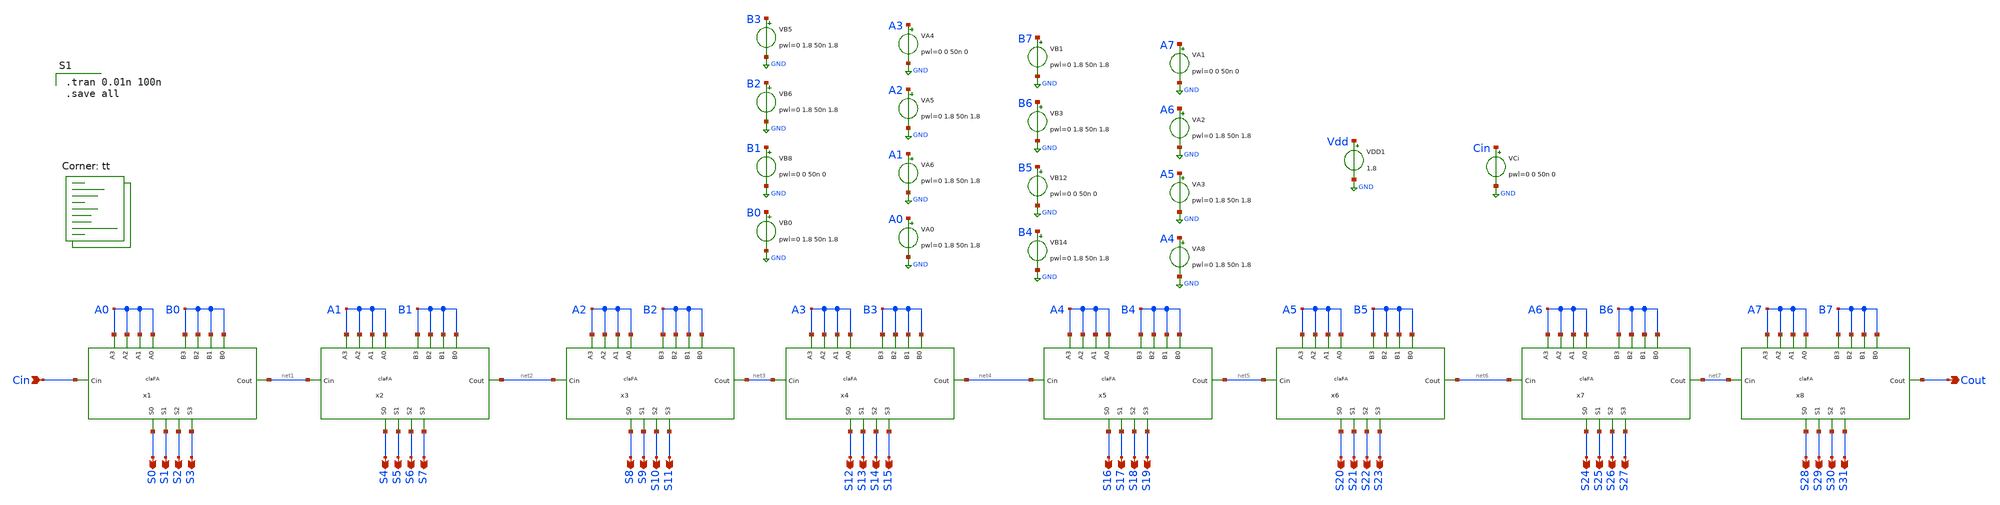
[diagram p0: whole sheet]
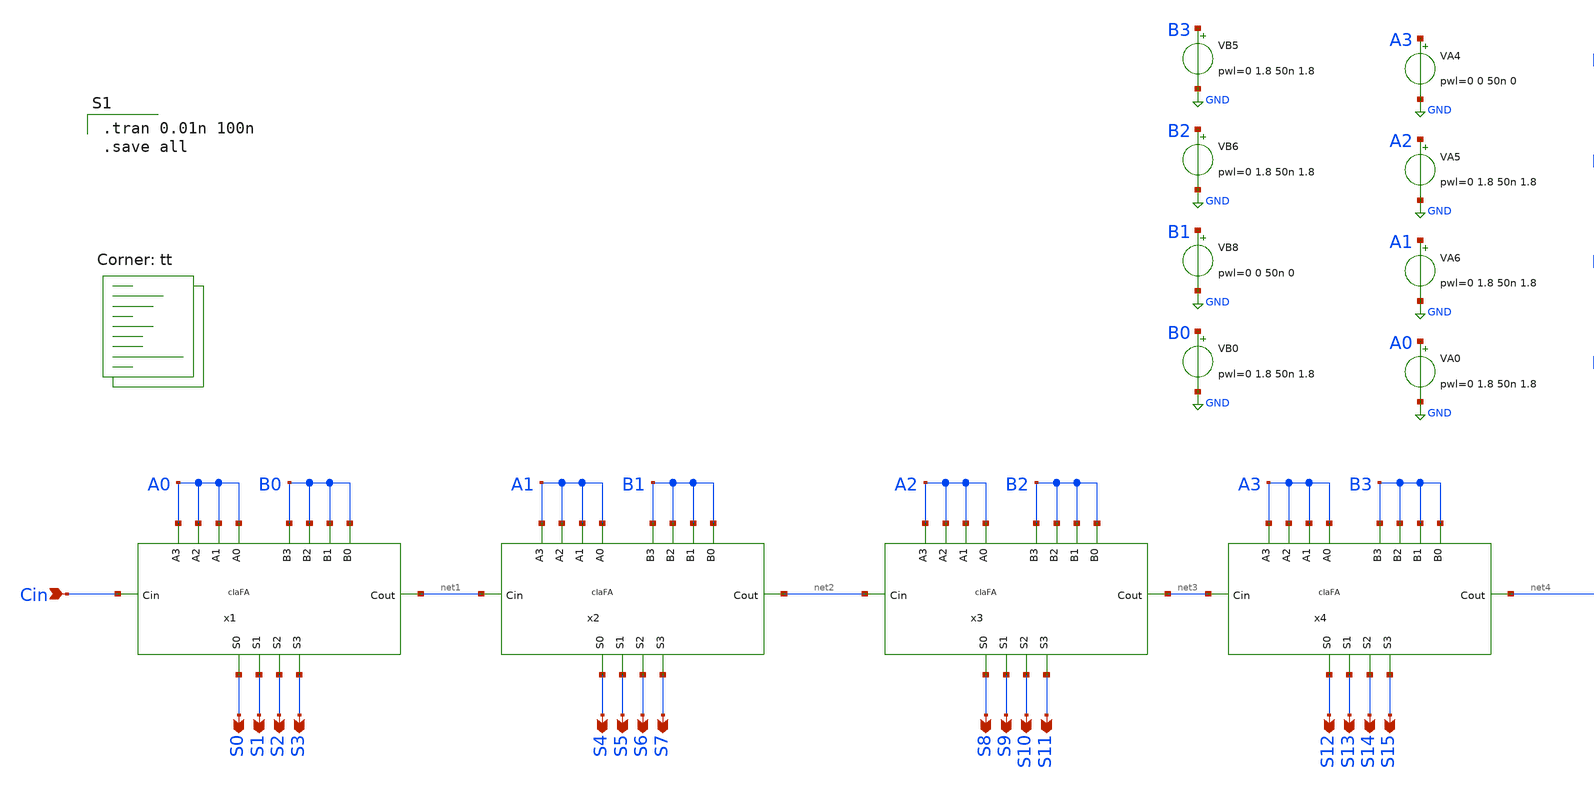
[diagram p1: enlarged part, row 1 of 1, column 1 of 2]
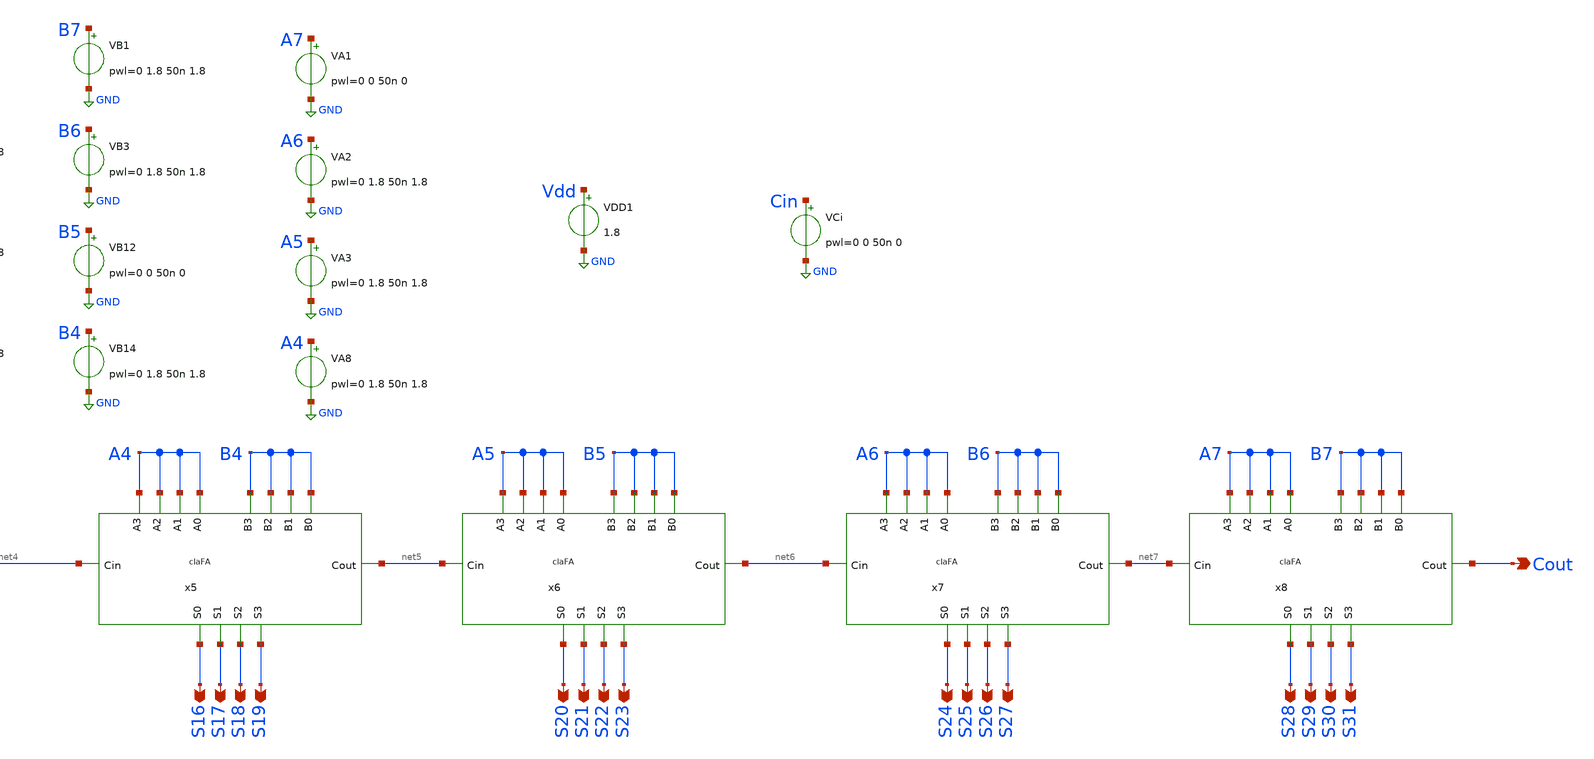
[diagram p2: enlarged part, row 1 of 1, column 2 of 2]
** sch_path: gates/32bit_CLA_FA_sim.sch
**.subckt 32bit_CLA_FA_sim Cin Cout S0 S1 S2 S3 S4 S5 S6 S7 S8 S9 S10 S11 S12 S13 S14 S15 S16 S17
*+ S18 S19 S20 S21 S22 S23 S24 S25 S26 S27 S28 S29 S30 S31
*.ipin Cin
*.opin Cout
*.opin S0
*.opin S1
*.opin S2
*.opin S3
*.opin S4
*.opin S5
*.opin S6
*.opin S7
*.opin S8
*.opin S9
*.opin S10
*.opin S11
*.opin S12
*.opin S13
*.opin S14
*.opin S15
*.opin S16
*.opin S17
*.opin S18
*.opin S19
*.opin S20
*.opin S21
*.opin S22
*.opin S23
*.opin S24
*.opin S25
*.opin S26
*.opin S27
*.opin S28
*.opin S29
*.opin S30
*.opin S31
x1 A0 A0 A0 A0 S2 B0 B0 B0 S1 S0 B0 S3 Cin net1 claFA
x2 A1 A1 A1 A1 S6 B1 B1 B1 S5 S4 B1 S7 net1 net2 claFA
x3 A2 A2 A2 A2 S10 B2 B2 B2 S9 S8 B2 S11 net2 net3 claFA
x4 A3 A3 A3 A3 S14 B3 B3 B3 S13 S12 B3 S15 net3 net4 claFA
VA4 A3 GND pwl=0 0 50n 0
VA5 A2 GND pwl=0 1.8 50n 1.8
VA6 A1 GND pwl=0 1.8 50n 1.8
VA0 A0 GND pwl=0 1.8 50n 1.8
VB5 B3 GND pwl=0 1.8 50n 1.8
VB6 B2 GND pwl=0 1.8 50n 1.8
VB8 B1 GND pwl=0 0 50n 0
VB0 B0 GND pwl=0 1.8 50n 1.8
VCi Cin GND pwl=0 0 50n 0
VDD1 Vdd GND 1.8
x5 A4 A4 A4 A4 S18 B4 B4 B4 S17 S16 B4 S19 net4 net5 claFA
x6 A5 A5 A5 A5 S22 B5 B5 B5 S21 S20 B5 S23 net5 net6 claFA
x7 A6 A6 A6 A6 S26 B6 B6 B6 S25 S24 B6 S27 net6 net7 claFA
x8 A7 A7 A7 A7 S30 B7 B7 B7 S29 S28 B7 S31 net7 Cout claFA
VA1 A7 GND pwl=0 0 50n 0
VA2 A6 GND pwl=0 1.8 50n 1.8
VA3 A5 GND pwl=0 1.8 50n 1.8
VA8 A4 GND pwl=0 1.8 50n 1.8
VB1 B7 GND pwl=0 1.8 50n 1.8
VB3 B6 GND pwl=0 1.8 50n 1.8
VB12 B5 GND pwl=0 0 50n 0
VB14 B4 GND pwl=0 1.8 50n 1.8
**** begin user architecture code

.tran 0.01n 100n
.save all

.lib $::SKYWATER_MODELS/sky130.lib.spice tt
**** end user architecture code
**.ends

* expanding   symbol:  claFA.sym # of pins=14
** sym_path: gates/claFA.sym
** sch_path: gates/claFA.sch
.subckt claFA A2 A0 A1 A3 S2 B2 B1 B0 S1 S0 B3 S3 Cin Cout
*.opin S0
*.ipin A0
*.ipin B0
*.ipin Cin
*.opin S1
*.ipin A1
*.ipin B1
*.opin S2
*.ipin A2
*.ipin B2
*.opin S3
*.ipin A3
*.ipin B3
*.opin Cout
x1 A0 B0 net3 XOR2
x2 net3 Cin S0 XOR2
x3 net1 Co1 net2 OR2
x4 Cin net1 net3 AND2
x5 A0 net2 B0 AND2
x6 A1 B1 net6 XOR2
x7 net6 C1 S1 XOR2
x8 net4 Co2 net5 OR2
x9 C1 net4 net6 AND2
x10 A1 net5 B1 AND2
x11 A2 B2 net9 XOR2
x12 net9 C2 S2 XOR2
x13 net7 Co3 net8 OR2
x14 C2 net7 net9 AND2
x15 A2 net8 B2 AND2
x16 A3 B3 net10 XOR2
x17 net10 C3 S3 XOR2
x18 net11 Co4 net12 OR2
x19 C3 net11 net10 AND2
x20 A3 net12 B3 AND2
x21 net6 net5 net10 net3 net9 net8 net12 Cin net2 C1 C2 C3 Cout 4_BIT_CLA_Carry_logic
.ends


* expanding   symbol:  XOR2.sym # of pins=3
** sym_path: gates/XOR2.sym
** sch_path: gates/XOR2.sch
.subckt XOR2 B A Y
*.ipin A
*.ipin B
*.opin Y
XM1 Y A net5 GND sky130_fd_pr__nfet_01v8 L=0.15 W=1 nf=1 ad='int((nf+1)/2) * W/nf * 0.29' as='int((nf+2)/2) * W/nf * 0.29'
+ pd='2*int((nf+1)/2) * (W/nf + 0.29)' ps='2*int((nf+2)/2) * (W/nf + 0.29)' nrd='0.29 / W' nrs='0.29 / W'
+ sa=0 sb=0 sd=0 mult=1 m=1
XM2 net5 B GND GND sky130_fd_pr__nfet_01v8 L=0.15 W=1 nf=1 ad='int((nf+1)/2) * W/nf * 0.29' as='int((nf+2)/2) * W/nf * 0.29'
+ pd='2*int((nf+1)/2) * (W/nf + 0.29)' ps='2*int((nf+2)/2) * (W/nf + 0.29)' nrd='0.29 / W' nrs='0.29 / W'
+ sa=0 sb=0 sd=0 mult=1 m=1
XM3 Y net1 net2 VDD sky130_fd_pr__pfet_01v8 L=0.15 W=1 nf=1 ad='int((nf+1)/2) * W/nf * 0.29' as='int((nf+2)/2) * W/nf * 0.29'
+ pd='2*int((nf+1)/2) * (W/nf + 0.29)' ps='2*int((nf+2)/2) * (W/nf + 0.29)' nrd='0.29 / W' nrs='0.29 / W'
+ sa=0 sb=0 sd=0 mult=1 m=1
XM4 net2 A VDD VDD sky130_fd_pr__pfet_01v8 L=0.15 W=1 nf=1 ad='int((nf+1)/2) * W/nf * 0.29' as='int((nf+2)/2) * W/nf * 0.29'
+ pd='2*int((nf+1)/2) * (W/nf + 0.29)' ps='2*int((nf+2)/2) * (W/nf + 0.29)' nrd='0.29 / W' nrs='0.29 / W'
+ sa=0 sb=0 sd=0 mult=1 m=1
XM5 net2 B VDD VDD sky130_fd_pr__pfet_01v8 L=0.15 W=1 nf=1 ad='int((nf+1)/2) * W/nf * 0.29' as='int((nf+2)/2) * W/nf * 0.29'
+ pd='2*int((nf+1)/2) * (W/nf + 0.29)' ps='2*int((nf+2)/2) * (W/nf + 0.29)' nrd='0.29 / W' nrs='0.29 / W'
+ sa=0 sb=0 sd=0 mult=1 m=1
XM6 Y net3 net2 VDD sky130_fd_pr__pfet_01v8 L=0.15 W=1 nf=1 ad='int((nf+1)/2) * W/nf * 0.29' as='int((nf+2)/2) * W/nf * 0.29'
+ pd='2*int((nf+1)/2) * (W/nf + 0.29)' ps='2*int((nf+2)/2) * (W/nf + 0.29)' nrd='0.29 / W' nrs='0.29 / W'
+ sa=0 sb=0 sd=0 mult=1 m=1
XM7 Y net1 net4 GND sky130_fd_pr__nfet_01v8 L=0.15 W=1 nf=1 ad='int((nf+1)/2) * W/nf * 0.29' as='int((nf+2)/2) * W/nf * 0.29'
+ pd='2*int((nf+1)/2) * (W/nf + 0.29)' ps='2*int((nf+2)/2) * (W/nf + 0.29)' nrd='0.29 / W' nrs='0.29 / W'
+ sa=0 sb=0 sd=0 mult=1 m=1
XM8 net4 net3 GND GND sky130_fd_pr__nfet_01v8 L=0.15 W=1 nf=1 ad='int((nf+1)/2) * W/nf * 0.29' as='int((nf+2)/2) * W/nf * 0.29'
+ pd='2*int((nf+1)/2) * (W/nf + 0.29)' ps='2*int((nf+2)/2) * (W/nf + 0.29)' nrd='0.29 / W' nrs='0.29 / W'
+ sa=0 sb=0 sd=0 mult=1 m=1
X1 A net1 inv_vtc
X2 B net3 inv_vtc
.ends


* expanding   symbol:  OR2.sym # of pins=3
** sym_path: gates/OR2.sym
** sch_path: gates/OR2.sch
.subckt OR2 B Y A
*.ipin A
*.ipin B
*.opin Y
XM7 VDD B net2 VDD sky130_fd_pr__pfet_01v8 L=0.15 W=1 nf=1 ad='int((nf+1)/2) * W/nf * 0.29' as='int((nf+2)/2) * W/nf * 0.29'
+ pd='2*int((nf+1)/2) * (W/nf + 0.29)' ps='2*int((nf+2)/2) * (W/nf + 0.29)' nrd='0.29 / W' nrs='0.29 / W'
+ sa=0 sb=0 sd=0 mult=1 m=1
XM8 GND B net1 GND sky130_fd_pr__nfet_01v8 L=0.15 W=1 nf=1 ad='int((nf+1)/2) * W/nf * 0.29' as='int((nf+2)/2) * W/nf * 0.29'
+ pd='2*int((nf+1)/2) * (W/nf + 0.29)' ps='2*int((nf+2)/2) * (W/nf + 0.29)' nrd='0.29 / W' nrs='0.29 / W'
+ sa=0 sb=0 sd=0 mult=1 m=1
XM9 net2 A net1 VDD sky130_fd_pr__pfet_01v8 L=0.15 W=1 nf=1 ad='int((nf+1)/2) * W/nf * 0.29' as='int((nf+2)/2) * W/nf * 0.29'
+ pd='2*int((nf+1)/2) * (W/nf + 0.29)' ps='2*int((nf+2)/2) * (W/nf + 0.29)' nrd='0.29 / W' nrs='0.29 / W'
+ sa=0 sb=0 sd=0 mult=1 m=1
XM10 GND A net1 GND sky130_fd_pr__nfet_01v8 L=0.15 W=1 nf=1 ad='int((nf+1)/2) * W/nf * 0.29' as='int((nf+2)/2) * W/nf * 0.29'
+ pd='2*int((nf+1)/2) * (W/nf + 0.29)' ps='2*int((nf+2)/2) * (W/nf + 0.29)' nrd='0.29 / W' nrs='0.29 / W'
+ sa=0 sb=0 sd=0 mult=1 m=1
X1 net1 Y inv_vtc
.ends


* expanding   symbol:  AND2.sym # of pins=3
** sym_path: gates/AND2.sym
** sch_path: gates/AND2.sch
.subckt AND2 A Y B
*.opin Y
*.ipin A
*.ipin B
x1 A net1 B NAND2_Gate
X2 net1 Y inv_vtc
.ends


* expanding   symbol:  4_BIT_CLA_Carry_logic.sym # of pins=13
** sym_path: gates/4_BIT_CLA_Carry_logic.sym
** sch_path: gates/4_BIT_CLA_Carry_logic.sch
.subckt 4_BIT_CLA_Carry_logic P1 G1 P3 P0 P2 G2 G3 Cin G0 C1 C2 C3 C4
*.ipin P0
*.ipin P1
*.ipin P2
*.ipin P3
*.ipin G0
*.ipin G1
*.ipin G2
*.ipin G3
*.ipin Cin
*.opin C1
*.opin C2
*.opin C3
*.opin C4
x5 Cin x5 P0 AND2
x6 G0 C1 x5 OR2
x7 G1 net1 net2 C2 OR3
x8 P1 net1 G0 AND2
x9 Cin net10 P0 P1 AND3
x1 G2 net3 net4 C3 net5 OR4
x2 P2 net3 G1 AND2
x3 P1 net11 P2 G0 AND3
x4 net12 net5 net13 net14 net15 AND4
x10 G3 net6 net7 net8 C4 net9 OR5
x12 P3 net6 G2 AND2
x13 net16 net17 net18 net19 AND3
x14 net20 net8 net21 net22 net23 AND4
x11 net24 net25 net26 net27 net28 net29 AND5
.ends


* expanding   symbol:  inv_vtc.sym # of pins=2
** sym_path: gates/inv_vtc.sym
** sch_path: gates/inv_vtc.sch
.subckt inv_vtc A Y
*.ipin A
*.opin Y
XM1 Y A VDD VDD sky130_fd_pr__pfet_01v8 L=0.15 W=2 nf=1 ad='int((nf+1)/2) * W/nf * 0.29' as='int((nf+2)/2) * W/nf * 0.29'
+ pd='2*int((nf+1)/2) * (W/nf + 0.29)' ps='2*int((nf+2)/2) * (W/nf + 0.29)' nrd='0.29 / W' nrs='0.29 / W'
+ sa=0 sb=0 sd=0 mult=1 m=1
XM2 Y A GND GND sky130_fd_pr__nfet_01v8 L=0.15 W=1 nf=1 ad='int((nf+1)/2) * W/nf * 0.29' as='int((nf+2)/2) * W/nf * 0.29'
+ pd='2*int((nf+1)/2) * (W/nf + 0.29)' ps='2*int((nf+2)/2) * (W/nf + 0.29)' nrd='0.29 / W' nrs='0.29 / W'
+ sa=0 sb=0 sd=0 mult=1 m=1
.ends


* expanding   symbol:  NAND2_Gate.sym # of pins=3
** sym_path: gates/NAND2_Gate.sym
** sch_path: gates/NAND2_Gate.sch
.subckt NAND2_Gate A Y B
*.ipin A
*.ipin B
*.opin Y
XM1 Y A net1 GND sky130_fd_pr__nfet_01v8 L=0.15 W=1 nf=1 ad='int((nf+1)/2) * W/nf * 0.29' as='int((nf+2)/2) * W/nf * 0.29'
+ pd='2*int((nf+1)/2) * (W/nf + 0.29)' ps='2*int((nf+2)/2) * (W/nf + 0.29)' nrd='0.29 / W' nrs='0.29 / W'
+ sa=0 sb=0 sd=0 mult=1 m=1
XM2 net1 B GND GND sky130_fd_pr__nfet_01v8 L=0.15 W=1 nf=1 ad='int((nf+1)/2) * W/nf * 0.29' as='int((nf+2)/2) * W/nf * 0.29'
+ pd='2*int((nf+1)/2) * (W/nf + 0.29)' ps='2*int((nf+2)/2) * (W/nf + 0.29)' nrd='0.29 / W' nrs='0.29 / W'
+ sa=0 sb=0 sd=0 mult=1 m=1
XM3 Y A VDD VDD sky130_fd_pr__pfet_01v8 L=0.15 W=1 nf=1 ad='int((nf+1)/2) * W/nf * 0.29' as='int((nf+2)/2) * W/nf * 0.29'
+ pd='2*int((nf+1)/2) * (W/nf + 0.29)' ps='2*int((nf+2)/2) * (W/nf + 0.29)' nrd='0.29 / W' nrs='0.29 / W'
+ sa=0 sb=0 sd=0 mult=1 m=1
XM4 Y B VDD VDD sky130_fd_pr__pfet_01v8 L=0.15 W=1 nf=1 ad='int((nf+1)/2) * W/nf * 0.29' as='int((nf+2)/2) * W/nf * 0.29'
+ pd='2*int((nf+1)/2) * (W/nf + 0.29)' ps='2*int((nf+2)/2) * (W/nf + 0.29)' nrd='0.29 / W' nrs='0.29 / W'
+ sa=0 sb=0 sd=0 mult=1 m=1
.ends


* expanding   symbol:  OR3.sym # of pins=4
** sym_path: gates/OR3.sym
** sch_path: gates/OR3.sch
.subckt OR3 C B A Y
*.ipin A
*.ipin B
*.opin Y
*.ipin C
XM5 VDD C net3 VDD sky130_fd_pr__pfet_01v8 L=0.15 W=1 nf=1 ad='int((nf+1)/2) * W/nf * 0.29' as='int((nf+2)/2) * W/nf * 0.29'
+ pd='2*int((nf+1)/2) * (W/nf + 0.29)' ps='2*int((nf+2)/2) * (W/nf + 0.29)' nrd='0.29 / W' nrs='0.29 / W'
+ sa=0 sb=0 sd=0 mult=1 m=1
XM6 GND C net1 GND sky130_fd_pr__nfet_01v8 L=0.15 W=1 nf=1 ad='int((nf+1)/2) * W/nf * 0.29' as='int((nf+2)/2) * W/nf * 0.29'
+ pd='2*int((nf+1)/2) * (W/nf + 0.29)' ps='2*int((nf+2)/2) * (W/nf + 0.29)' nrd='0.29 / W' nrs='0.29 / W'
+ sa=0 sb=0 sd=0 mult=1 m=1
XM7 net3 B net2 VDD sky130_fd_pr__pfet_01v8 L=0.15 W=1 nf=1 ad='int((nf+1)/2) * W/nf * 0.29' as='int((nf+2)/2) * W/nf * 0.29'
+ pd='2*int((nf+1)/2) * (W/nf + 0.29)' ps='2*int((nf+2)/2) * (W/nf + 0.29)' nrd='0.29 / W' nrs='0.29 / W'
+ sa=0 sb=0 sd=0 mult=1 m=1
XM8 GND B net1 GND sky130_fd_pr__nfet_01v8 L=0.15 W=1 nf=1 ad='int((nf+1)/2) * W/nf * 0.29' as='int((nf+2)/2) * W/nf * 0.29'
+ pd='2*int((nf+1)/2) * (W/nf + 0.29)' ps='2*int((nf+2)/2) * (W/nf + 0.29)' nrd='0.29 / W' nrs='0.29 / W'
+ sa=0 sb=0 sd=0 mult=1 m=1
XM9 net2 A net1 VDD sky130_fd_pr__pfet_01v8 L=0.15 W=1 nf=1 ad='int((nf+1)/2) * W/nf * 0.29' as='int((nf+2)/2) * W/nf * 0.29'
+ pd='2*int((nf+1)/2) * (W/nf + 0.29)' ps='2*int((nf+2)/2) * (W/nf + 0.29)' nrd='0.29 / W' nrs='0.29 / W'
+ sa=0 sb=0 sd=0 mult=1 m=1
XM10 GND A net1 GND sky130_fd_pr__nfet_01v8 L=0.15 W=1 nf=1 ad='int((nf+1)/2) * W/nf * 0.29' as='int((nf+2)/2) * W/nf * 0.29'
+ pd='2*int((nf+1)/2) * (W/nf + 0.29)' ps='2*int((nf+2)/2) * (W/nf + 0.29)' nrd='0.29 / W' nrs='0.29 / W'
+ sa=0 sb=0 sd=0 mult=1 m=1
X1 net1 Y inv_vtc
.ends


* expanding   symbol:  AND3.sym # of pins=4
** sym_path: gates/AND3.sym
** sch_path: gates/AND3.sch
.subckt AND3 A Y B c
*.ipin A
*.ipin B
*.opin Y
*.ipin c
XM1 net1 A net2 GND sky130_fd_pr__nfet_01v8 L=0.15 W=1 nf=1 ad='int((nf+1)/2) * W/nf * 0.29' as='int((nf+2)/2) * W/nf * 0.29'
+ pd='2*int((nf+1)/2) * (W/nf + 0.29)' ps='2*int((nf+2)/2) * (W/nf + 0.29)' nrd='0.29 / W' nrs='0.29 / W'
+ sa=0 sb=0 sd=0 mult=1 m=1
XM2 net2 B net3 GND sky130_fd_pr__nfet_01v8 L=0.15 W=1 nf=1 ad='int((nf+1)/2) * W/nf * 0.29' as='int((nf+2)/2) * W/nf * 0.29'
+ pd='2*int((nf+1)/2) * (W/nf + 0.29)' ps='2*int((nf+2)/2) * (W/nf + 0.29)' nrd='0.29 / W' nrs='0.29 / W'
+ sa=0 sb=0 sd=0 mult=1 m=1
XM3 net1 A VDD VDD sky130_fd_pr__pfet_01v8 L=0.15 W=1 nf=1 ad='int((nf+1)/2) * W/nf * 0.29' as='int((nf+2)/2) * W/nf * 0.29'
+ pd='2*int((nf+1)/2) * (W/nf + 0.29)' ps='2*int((nf+2)/2) * (W/nf + 0.29)' nrd='0.29 / W' nrs='0.29 / W'
+ sa=0 sb=0 sd=0 mult=1 m=1
XM4 net1 B VDD VDD sky130_fd_pr__pfet_01v8 L=0.15 W=1 nf=1 ad='int((nf+1)/2) * W/nf * 0.29' as='int((nf+2)/2) * W/nf * 0.29'
+ pd='2*int((nf+1)/2) * (W/nf + 0.29)' ps='2*int((nf+2)/2) * (W/nf + 0.29)' nrd='0.29 / W' nrs='0.29 / W'
+ sa=0 sb=0 sd=0 mult=1 m=1
XM5 net1 c VDD VDD sky130_fd_pr__pfet_01v8 L=0.15 W=1 nf=1 ad='int((nf+1)/2) * W/nf * 0.29' as='int((nf+2)/2) * W/nf * 0.29'
+ pd='2*int((nf+1)/2) * (W/nf + 0.29)' ps='2*int((nf+2)/2) * (W/nf + 0.29)' nrd='0.29 / W' nrs='0.29 / W'
+ sa=0 sb=0 sd=0 mult=1 m=1
XM6 net3 c GND GND sky130_fd_pr__nfet_01v8 L=0.15 W=1 nf=1 ad='int((nf+1)/2) * W/nf * 0.29' as='int((nf+2)/2) * W/nf * 0.29'
+ pd='2*int((nf+1)/2) * (W/nf + 0.29)' ps='2*int((nf+2)/2) * (W/nf + 0.29)' nrd='0.29 / W' nrs='0.29 / W'
+ sa=0 sb=0 sd=0 mult=1 m=1
X1 net1 Y inv_vtc
.ends


* expanding   symbol:  OR4.sym # of pins=5
** sym_path: gates/OR4.sym
** sch_path: gates/OR4.sch
.subckt OR4 D C B Y A
*.ipin A
*.ipin B
*.opin Y
*.ipin C
*.ipin D
XM2 GND D net1 GND sky130_fd_pr__nfet_01v8 L=0.15 W=1 nf=1 ad='int((nf+1)/2) * W/nf * 0.29' as='int((nf+2)/2) * W/nf * 0.29'
+ pd='2*int((nf+1)/2) * (W/nf + 0.29)' ps='2*int((nf+2)/2) * (W/nf + 0.29)' nrd='0.29 / W' nrs='0.29 / W'
+ sa=0 sb=0 sd=0 mult=1 m=1
XM4 VDD D net4 VDD sky130_fd_pr__pfet_01v8 L=0.15 W=1 nf=1 ad='int((nf+1)/2) * W/nf * 0.29' as='int((nf+2)/2) * W/nf * 0.29'
+ pd='2*int((nf+1)/2) * (W/nf + 0.29)' ps='2*int((nf+2)/2) * (W/nf + 0.29)' nrd='0.29 / W' nrs='0.29 / W'
+ sa=0 sb=0 sd=0 mult=1 m=1
XM5 net4 C net3 VDD sky130_fd_pr__pfet_01v8 L=0.15 W=1 nf=1 ad='int((nf+1)/2) * W/nf * 0.29' as='int((nf+2)/2) * W/nf * 0.29'
+ pd='2*int((nf+1)/2) * (W/nf + 0.29)' ps='2*int((nf+2)/2) * (W/nf + 0.29)' nrd='0.29 / W' nrs='0.29 / W'
+ sa=0 sb=0 sd=0 mult=1 m=1
XM6 GND C net1 GND sky130_fd_pr__nfet_01v8 L=0.15 W=1 nf=1 ad='int((nf+1)/2) * W/nf * 0.29' as='int((nf+2)/2) * W/nf * 0.29'
+ pd='2*int((nf+1)/2) * (W/nf + 0.29)' ps='2*int((nf+2)/2) * (W/nf + 0.29)' nrd='0.29 / W' nrs='0.29 / W'
+ sa=0 sb=0 sd=0 mult=1 m=1
XM7 net3 B net2 VDD sky130_fd_pr__pfet_01v8 L=0.15 W=1 nf=1 ad='int((nf+1)/2) * W/nf * 0.29' as='int((nf+2)/2) * W/nf * 0.29'
+ pd='2*int((nf+1)/2) * (W/nf + 0.29)' ps='2*int((nf+2)/2) * (W/nf + 0.29)' nrd='0.29 / W' nrs='0.29 / W'
+ sa=0 sb=0 sd=0 mult=1 m=1
XM8 GND B net1 GND sky130_fd_pr__nfet_01v8 L=0.15 W=1 nf=1 ad='int((nf+1)/2) * W/nf * 0.29' as='int((nf+2)/2) * W/nf * 0.29'
+ pd='2*int((nf+1)/2) * (W/nf + 0.29)' ps='2*int((nf+2)/2) * (W/nf + 0.29)' nrd='0.29 / W' nrs='0.29 / W'
+ sa=0 sb=0 sd=0 mult=1 m=1
XM9 net2 A net1 VDD sky130_fd_pr__pfet_01v8 L=0.15 W=1 nf=1 ad='int((nf+1)/2) * W/nf * 0.29' as='int((nf+2)/2) * W/nf * 0.29'
+ pd='2*int((nf+1)/2) * (W/nf + 0.29)' ps='2*int((nf+2)/2) * (W/nf + 0.29)' nrd='0.29 / W' nrs='0.29 / W'
+ sa=0 sb=0 sd=0 mult=1 m=1
XM10 GND A net1 GND sky130_fd_pr__nfet_01v8 L=0.15 W=1 nf=1 ad='int((nf+1)/2) * W/nf * 0.29' as='int((nf+2)/2) * W/nf * 0.29'
+ pd='2*int((nf+1)/2) * (W/nf + 0.29)' ps='2*int((nf+2)/2) * (W/nf + 0.29)' nrd='0.29 / W' nrs='0.29 / W'
+ sa=0 sb=0 sd=0 mult=1 m=1
X2 net1 Y inv_vtc
.ends


* expanding   symbol:  AND4.sym # of pins=5
** sym_path: gates/AND4.sym
** sch_path: gates/AND4.sch
.subckt AND4 A Y B C D
*.ipin A
*.ipin B
*.opin Y
*.ipin C
*.ipin D
XM1 net1 A net2 GND sky130_fd_pr__nfet_01v8 L=0.15 W=1 nf=1 ad='int((nf+1)/2) * W/nf * 0.29' as='int((nf+2)/2) * W/nf * 0.29'
+ pd='2*int((nf+1)/2) * (W/nf + 0.29)' ps='2*int((nf+2)/2) * (W/nf + 0.29)' nrd='0.29 / W' nrs='0.29 / W'
+ sa=0 sb=0 sd=0 mult=1 m=1
XM2 net2 B net3 GND sky130_fd_pr__nfet_01v8 L=0.15 W=1 nf=1 ad='int((nf+1)/2) * W/nf * 0.29' as='int((nf+2)/2) * W/nf * 0.29'
+ pd='2*int((nf+1)/2) * (W/nf + 0.29)' ps='2*int((nf+2)/2) * (W/nf + 0.29)' nrd='0.29 / W' nrs='0.29 / W'
+ sa=0 sb=0 sd=0 mult=1 m=1
XM3 net1 A VDD VDD sky130_fd_pr__pfet_01v8 L=0.15 W=1 nf=1 ad='int((nf+1)/2) * W/nf * 0.29' as='int((nf+2)/2) * W/nf * 0.29'
+ pd='2*int((nf+1)/2) * (W/nf + 0.29)' ps='2*int((nf+2)/2) * (W/nf + 0.29)' nrd='0.29 / W' nrs='0.29 / W'
+ sa=0 sb=0 sd=0 mult=1 m=1
XM4 net1 B VDD VDD sky130_fd_pr__pfet_01v8 L=0.15 W=1 nf=1 ad='int((nf+1)/2) * W/nf * 0.29' as='int((nf+2)/2) * W/nf * 0.29'
+ pd='2*int((nf+1)/2) * (W/nf + 0.29)' ps='2*int((nf+2)/2) * (W/nf + 0.29)' nrd='0.29 / W' nrs='0.29 / W'
+ sa=0 sb=0 sd=0 mult=1 m=1
XM5 net1 C VDD VDD sky130_fd_pr__pfet_01v8 L=0.15 W=1 nf=1 ad='int((nf+1)/2) * W/nf * 0.29' as='int((nf+2)/2) * W/nf * 0.29'
+ pd='2*int((nf+1)/2) * (W/nf + 0.29)' ps='2*int((nf+2)/2) * (W/nf + 0.29)' nrd='0.29 / W' nrs='0.29 / W'
+ sa=0 sb=0 sd=0 mult=1 m=1
XM6 net3 C net4 GND sky130_fd_pr__nfet_01v8 L=0.15 W=1 nf=1 ad='int((nf+1)/2) * W/nf * 0.29' as='int((nf+2)/2) * W/nf * 0.29'
+ pd='2*int((nf+1)/2) * (W/nf + 0.29)' ps='2*int((nf+2)/2) * (W/nf + 0.29)' nrd='0.29 / W' nrs='0.29 / W'
+ sa=0 sb=0 sd=0 mult=1 m=1
XM7 net1 D VDD VDD sky130_fd_pr__pfet_01v8 L=0.15 W=1 nf=1 ad='int((nf+1)/2) * W/nf * 0.29' as='int((nf+2)/2) * W/nf * 0.29'
+ pd='2*int((nf+1)/2) * (W/nf + 0.29)' ps='2*int((nf+2)/2) * (W/nf + 0.29)' nrd='0.29 / W' nrs='0.29 / W'
+ sa=0 sb=0 sd=0 mult=1 m=1
XM8 net4 D GND GND sky130_fd_pr__nfet_01v8 L=0.15 W=1 nf=1 ad='int((nf+1)/2) * W/nf * 0.29' as='int((nf+2)/2) * W/nf * 0.29'
+ pd='2*int((nf+1)/2) * (W/nf + 0.29)' ps='2*int((nf+2)/2) * (W/nf + 0.29)' nrd='0.29 / W' nrs='0.29 / W'
+ sa=0 sb=0 sd=0 mult=1 m=1
X1 net1 Y inv_vtc
.ends


* expanding   symbol:  OR5.sym # of pins=6
** sym_path: gates/OR5.sym
** sch_path: gates/OR5.sch
.subckt OR5 E D C B Y A
*.ipin A
*.ipin B
*.opin Y
*.ipin C
*.ipin D
*.ipin E
XM1 GND E net1 GND sky130_fd_pr__nfet_01v8 L=0.15 W=1 nf=1 ad='int((nf+1)/2) * W/nf * 0.29' as='int((nf+2)/2) * W/nf * 0.29'
+ pd='2*int((nf+1)/2) * (W/nf + 0.29)' ps='2*int((nf+2)/2) * (W/nf + 0.29)' nrd='0.29 / W' nrs='0.29 / W'
+ sa=0 sb=0 sd=0 mult=1 m=1
XM2 GND D net1 GND sky130_fd_pr__nfet_01v8 L=0.15 W=1 nf=1 ad='int((nf+1)/2) * W/nf * 0.29' as='int((nf+2)/2) * W/nf * 0.29'
+ pd='2*int((nf+1)/2) * (W/nf + 0.29)' ps='2*int((nf+2)/2) * (W/nf + 0.29)' nrd='0.29 / W' nrs='0.29 / W'
+ sa=0 sb=0 sd=0 mult=1 m=1
XM3 VDD E VDD VDD sky130_fd_pr__pfet_01v8 L=0.15 W=1 nf=1 ad='int((nf+1)/2) * W/nf * 0.29' as='int((nf+2)/2) * W/nf * 0.29'
+ pd='2*int((nf+1)/2) * (W/nf + 0.29)' ps='2*int((nf+2)/2) * (W/nf + 0.29)' nrd='0.29 / W' nrs='0.29 / W'
+ sa=0 sb=0 sd=0 mult=1 m=1
XM4 VDD D net4 VDD sky130_fd_pr__pfet_01v8 L=0.15 W=1 nf=1 ad='int((nf+1)/2) * W/nf * 0.29' as='int((nf+2)/2) * W/nf * 0.29'
+ pd='2*int((nf+1)/2) * (W/nf + 0.29)' ps='2*int((nf+2)/2) * (W/nf + 0.29)' nrd='0.29 / W' nrs='0.29 / W'
+ sa=0 sb=0 sd=0 mult=1 m=1
XM5 net4 C net3 VDD sky130_fd_pr__pfet_01v8 L=0.15 W=1 nf=1 ad='int((nf+1)/2) * W/nf * 0.29' as='int((nf+2)/2) * W/nf * 0.29'
+ pd='2*int((nf+1)/2) * (W/nf + 0.29)' ps='2*int((nf+2)/2) * (W/nf + 0.29)' nrd='0.29 / W' nrs='0.29 / W'
+ sa=0 sb=0 sd=0 mult=1 m=1
XM6 GND C net1 GND sky130_fd_pr__nfet_01v8 L=0.15 W=1 nf=1 ad='int((nf+1)/2) * W/nf * 0.29' as='int((nf+2)/2) * W/nf * 0.29'
+ pd='2*int((nf+1)/2) * (W/nf + 0.29)' ps='2*int((nf+2)/2) * (W/nf + 0.29)' nrd='0.29 / W' nrs='0.29 / W'
+ sa=0 sb=0 sd=0 mult=1 m=1
XM7 net3 B net2 VDD sky130_fd_pr__pfet_01v8 L=0.15 W=1 nf=1 ad='int((nf+1)/2) * W/nf * 0.29' as='int((nf+2)/2) * W/nf * 0.29'
+ pd='2*int((nf+1)/2) * (W/nf + 0.29)' ps='2*int((nf+2)/2) * (W/nf + 0.29)' nrd='0.29 / W' nrs='0.29 / W'
+ sa=0 sb=0 sd=0 mult=1 m=1
XM8 GND B net1 GND sky130_fd_pr__nfet_01v8 L=0.15 W=1 nf=1 ad='int((nf+1)/2) * W/nf * 0.29' as='int((nf+2)/2) * W/nf * 0.29'
+ pd='2*int((nf+1)/2) * (W/nf + 0.29)' ps='2*int((nf+2)/2) * (W/nf + 0.29)' nrd='0.29 / W' nrs='0.29 / W'
+ sa=0 sb=0 sd=0 mult=1 m=1
XM9 net2 A net1 VDD sky130_fd_pr__pfet_01v8 L=0.15 W=1 nf=1 ad='int((nf+1)/2) * W/nf * 0.29' as='int((nf+2)/2) * W/nf * 0.29'
+ pd='2*int((nf+1)/2) * (W/nf + 0.29)' ps='2*int((nf+2)/2) * (W/nf + 0.29)' nrd='0.29 / W' nrs='0.29 / W'
+ sa=0 sb=0 sd=0 mult=1 m=1
XM10 GND A net1 GND sky130_fd_pr__nfet_01v8 L=0.15 W=1 nf=1 ad='int((nf+1)/2) * W/nf * 0.29' as='int((nf+2)/2) * W/nf * 0.29'
+ pd='2*int((nf+1)/2) * (W/nf + 0.29)' ps='2*int((nf+2)/2) * (W/nf + 0.29)' nrd='0.29 / W' nrs='0.29 / W'
+ sa=0 sb=0 sd=0 mult=1 m=1
X2 net1 Y inv_vtc
.ends


* expanding   symbol:  AND5.sym # of pins=6
** sym_path: gates/AND5.sym
** sch_path: gates/AND5.sch
.subckt AND5 A Y B C D E
*.ipin A
*.ipin B
*.opin Y
*.ipin C
*.ipin D
*.ipin E
XM1 net1 A net2 GND sky130_fd_pr__nfet_01v8 L=0.15 W=1 nf=1 ad='int((nf+1)/2) * W/nf * 0.29' as='int((nf+2)/2) * W/nf * 0.29'
+ pd='2*int((nf+1)/2) * (W/nf + 0.29)' ps='2*int((nf+2)/2) * (W/nf + 0.29)' nrd='0.29 / W' nrs='0.29 / W'
+ sa=0 sb=0 sd=0 mult=1 m=1
XM2 net2 B net3 GND sky130_fd_pr__nfet_01v8 L=0.15 W=1 nf=1 ad='int((nf+1)/2) * W/nf * 0.29' as='int((nf+2)/2) * W/nf * 0.29'
+ pd='2*int((nf+1)/2) * (W/nf + 0.29)' ps='2*int((nf+2)/2) * (W/nf + 0.29)' nrd='0.29 / W' nrs='0.29 / W'
+ sa=0 sb=0 sd=0 mult=1 m=1
XM3 net1 A VDD VDD sky130_fd_pr__pfet_01v8 L=0.15 W=1 nf=1 ad='int((nf+1)/2) * W/nf * 0.29' as='int((nf+2)/2) * W/nf * 0.29'
+ pd='2*int((nf+1)/2) * (W/nf + 0.29)' ps='2*int((nf+2)/2) * (W/nf + 0.29)' nrd='0.29 / W' nrs='0.29 / W'
+ sa=0 sb=0 sd=0 mult=1 m=1
XM4 net1 B VDD VDD sky130_fd_pr__pfet_01v8 L=0.15 W=1 nf=1 ad='int((nf+1)/2) * W/nf * 0.29' as='int((nf+2)/2) * W/nf * 0.29'
+ pd='2*int((nf+1)/2) * (W/nf + 0.29)' ps='2*int((nf+2)/2) * (W/nf + 0.29)' nrd='0.29 / W' nrs='0.29 / W'
+ sa=0 sb=0 sd=0 mult=1 m=1
XM5 net1 C VDD VDD sky130_fd_pr__pfet_01v8 L=0.15 W=1 nf=1 ad='int((nf+1)/2) * W/nf * 0.29' as='int((nf+2)/2) * W/nf * 0.29'
+ pd='2*int((nf+1)/2) * (W/nf + 0.29)' ps='2*int((nf+2)/2) * (W/nf + 0.29)' nrd='0.29 / W' nrs='0.29 / W'
+ sa=0 sb=0 sd=0 mult=1 m=1
XM6 net3 C net4 GND sky130_fd_pr__nfet_01v8 L=0.15 W=1 nf=1 ad='int((nf+1)/2) * W/nf * 0.29' as='int((nf+2)/2) * W/nf * 0.29'
+ pd='2*int((nf+1)/2) * (W/nf + 0.29)' ps='2*int((nf+2)/2) * (W/nf + 0.29)' nrd='0.29 / W' nrs='0.29 / W'
+ sa=0 sb=0 sd=0 mult=1 m=1
XM7 net1 D VDD VDD sky130_fd_pr__pfet_01v8 L=0.15 W=1 nf=1 ad='int((nf+1)/2) * W/nf * 0.29' as='int((nf+2)/2) * W/nf * 0.29'
+ pd='2*int((nf+1)/2) * (W/nf + 0.29)' ps='2*int((nf+2)/2) * (W/nf + 0.29)' nrd='0.29 / W' nrs='0.29 / W'
+ sa=0 sb=0 sd=0 mult=1 m=1
XM8 net4 D GND GND sky130_fd_pr__nfet_01v8 L=0.15 W=1 nf=1 ad='int((nf+1)/2) * W/nf * 0.29' as='int((nf+2)/2) * W/nf * 0.29'
+ pd='2*int((nf+1)/2) * (W/nf + 0.29)' ps='2*int((nf+2)/2) * (W/nf + 0.29)' nrd='0.29 / W' nrs='0.29 / W'
+ sa=0 sb=0 sd=0 mult=1 m=1
XM9 net1 E VDD VDD sky130_fd_pr__pfet_01v8 L=0.15 W=1 nf=1 ad='int((nf+1)/2) * W/nf * 0.29' as='int((nf+2)/2) * W/nf * 0.29'
+ pd='2*int((nf+1)/2) * (W/nf + 0.29)' ps='2*int((nf+2)/2) * (W/nf + 0.29)' nrd='0.29 / W' nrs='0.29 / W'
+ sa=0 sb=0 sd=0 mult=1 m=1
XM10 GND E GND GND sky130_fd_pr__nfet_01v8 L=0.15 W=1 nf=1 ad='int((nf+1)/2) * W/nf * 0.29' as='int((nf+2)/2) * W/nf * 0.29'
+ pd='2*int((nf+1)/2) * (W/nf + 0.29)' ps='2*int((nf+2)/2) * (W/nf + 0.29)' nrd='0.29 / W' nrs='0.29 / W'
+ sa=0 sb=0 sd=0 mult=1 m=1
X1 net1 Y inv_vtc
.ends

.GLOBAL GND
.GLOBAL VDD
.end
